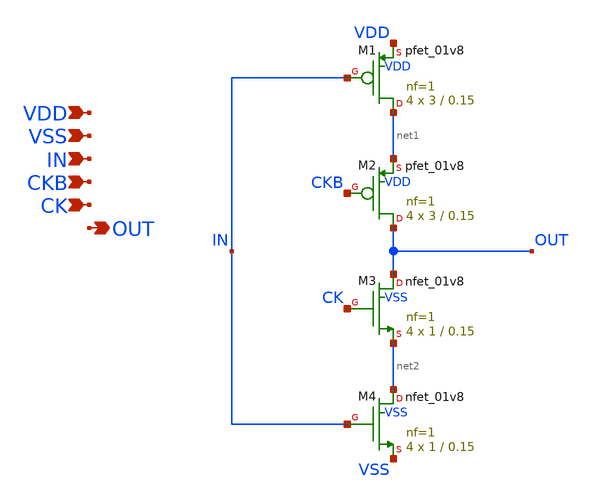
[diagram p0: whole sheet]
** sch_path: xschem/bsw.sch
**.subckt bsw VDD VSS IN CKB CK OUT
*.ipin VDD
*.ipin VSS
*.ipin IN
*.ipin CKB
*.ipin CK
*.opin OUT
XM1 net1 IN VDD VDD sky130_fd_pr__pfet_01v8 L=0.15 W=3 nf=1 ad='int((nf+1)/2) * W/nf * 0.29' as='int((nf+2)/2) * W/nf * 0.29'
+ pd='2*int((nf+1)/2) * (W/nf + 0.29)' ps='2*int((nf+2)/2) * (W/nf + 0.29)' nrd='0.29 / W' nrs='0.29 / W'
+ sa=0 sb=0 sd=0 mult=4 m=4
XM2 OUT CKB net1 VDD sky130_fd_pr__pfet_01v8 L=0.15 W=3 nf=1 ad='int((nf+1)/2) * W/nf * 0.29' as='int((nf+2)/2) * W/nf * 0.29'
+ pd='2*int((nf+1)/2) * (W/nf + 0.29)' ps='2*int((nf+2)/2) * (W/nf + 0.29)' nrd='0.29 / W' nrs='0.29 / W'
+ sa=0 sb=0 sd=0 mult=4 m=4
XM3 OUT CK net2 VSS sky130_fd_pr__nfet_01v8 L=0.15 W=1 nf=1 ad='int((nf+1)/2) * W/nf * 0.29' as='int((nf+2)/2) * W/nf * 0.29'
+ pd='2*int((nf+1)/2) * (W/nf + 0.29)' ps='2*int((nf+2)/2) * (W/nf + 0.29)' nrd='0.29 / W' nrs='0.29 / W'
+ sa=0 sb=0 sd=0 mult=4 m=4
XM4 net2 IN VSS VSS sky130_fd_pr__nfet_01v8 L=0.15 W=1 nf=1 ad='int((nf+1)/2) * W/nf * 0.29' as='int((nf+2)/2) * W/nf * 0.29'
+ pd='2*int((nf+1)/2) * (W/nf + 0.29)' ps='2*int((nf+2)/2) * (W/nf + 0.29)' nrd='0.29 / W' nrs='0.29 / W'
+ sa=0 sb=0 sd=0 mult=4 m=4
**.ends
.end
